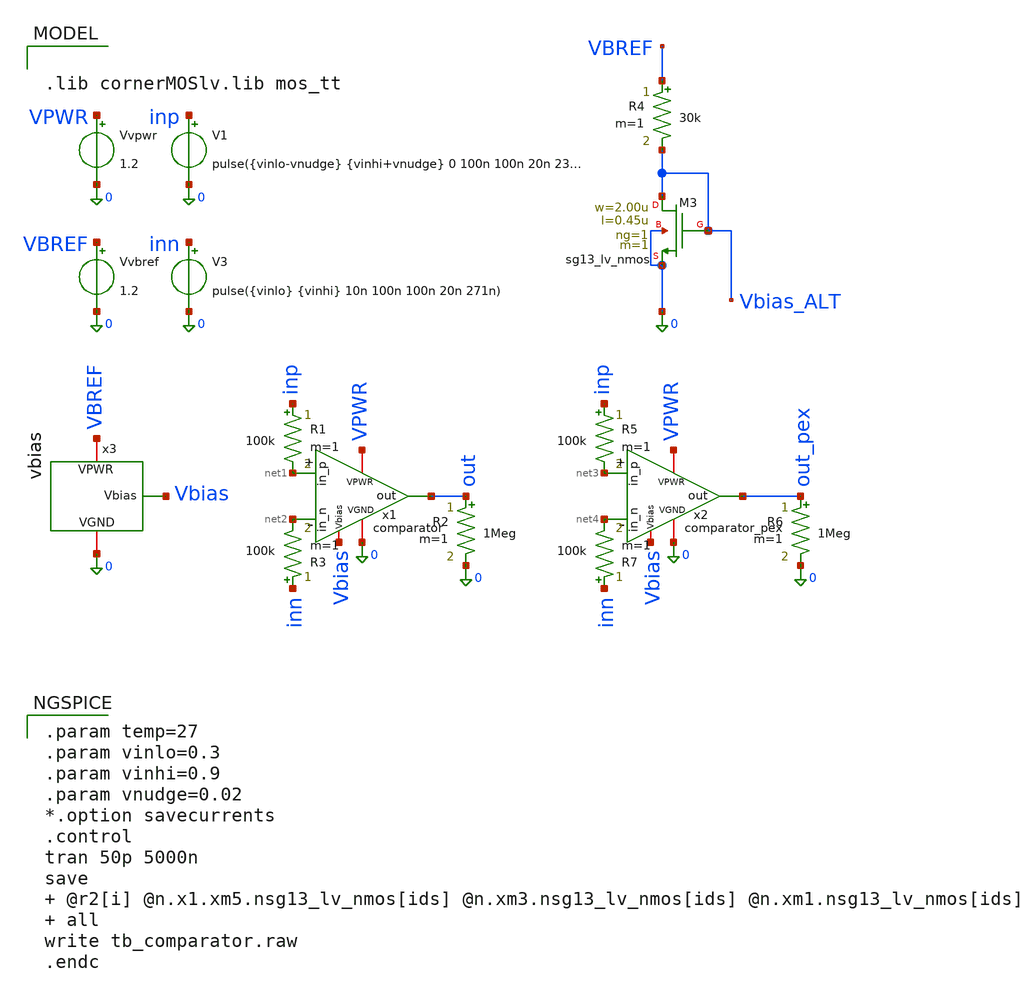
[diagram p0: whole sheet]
** sch_path: xschem/tb_comparator.sch
**.subckt tb_comparator
V1 inp 0 pulse({vinlo-vnudge} {vinhi+vnudge} 0 100n 100n 20n 239n)
R1 inp net1 100k m=1
R2 out 0 1Meg m=1
Vvpwr VPWR 0 1.2
x1 VPWR 0 out net2 net1 Vbias comparator
R3 inn net2 100k m=1
V3 inn 0 pulse({vinlo} {vinhi} 10n 100n 100n 20n 271n)
XM3 Vbias_ALT Vbias_ALT 0 0 sg13_lv_nmos w=2.00u l=0.45u ng=1 m=1 mm_ok=1
Vvbref VBREF 0 1.2
R4 VBREF Vbias_ALT 30k m=1
R5 inp net3 100k m=1
R6 out_pex 0 1Meg m=1
x2 VPWR 0 out_pex net4 net3 Vbias comparator_pex
R7 inn net4 100k m=1
x3 VBREF 0 Vbias vbias
**** begin user architecture code

.lib cornerMOSlv.lib mos_tt


.param temp=27
.param vinlo=0.3
.param vinhi=0.9
.param vnudge=0.02
*.option savecurrents
.control
tran 50p 5000n
save  @r2[i] @n.x1.xm5.nsg13_lv_nmos[ids] @n.xm3.nsg13_lv_nmos[ids] @n.xm1.nsg13_lv_nmos[ids]  all
write tb_comparator.raw
.endc


**** end user architecture code
**.ends

* expanding   symbol:  comparator.sym # of pins=6
** sym_path: xschem/comparator.sym
** sch_path: xschem/comparator.sch
.subckt comparator VPWR VGND out in_n in_p Vbias
*.iopin VPWR
*.ipin in_p
*.ipin in_n
*.opin out
*.iopin VGND
*.ipin Vbias
XM1 net2 in_p net1 VGND sg13_lv_nmos w=4.00u l=0.26u ng=1 m=1 mm_ok=1
XM4 diff net2 VPWR VPWR sg13_lv_pmos w=8.00u l=0.26u ng=1 m=1 mm_ok=1
XM5 net1 Vbias VGND VGND sg13_lv_nmos w=2.00u l=0.39u ng=1 m=1 mm_ok=1
XM2 diff in_n net1 VGND sg13_lv_nmos w=4.00u l=0.26u ng=1 m=1 mm_ok=1
XM3 net2 net2 VPWR VPWR sg13_lv_pmos w=8.00u l=0.26u ng=1 m=1 mm_ok=1
XM6 diff_amp diff VPWR VPWR sg13_lv_pmos w=8.00u l=0.26u ng=1 m=1 mm_ok=1
XM7 diff_amp Vbias VGND VGND sg13_lv_nmos w=2.00u l=0.39u ng=1 m=1 mm_ok=1
XM8 out diff_amp VPWR VPWR sg13_lv_pmos w=1.20u l=0.13u ng=1 m=1 mm_ok=1
XM9 out diff_amp VGND VGND sg13_lv_nmos w=0.50u l=0.13u ng=1 m=1 mm_ok=1
.ends


* expanding   symbol:  comparator_pex.sym # of pins=6
** sym_path: xschem/comparator.sym
.include [file normalize ../magic/comparator.sim.spice]

* expanding   symbol:  vbias.sym # of pins=3
** sym_path: xschem/vbias.sym
** sch_path: xschem/vbias.sch
.subckt vbias VPWR VGND Vbias
*.iopin VPWR
*.opin Vbias
*.iopin VGND
XM1 Vbias Vbias VGND VGND sg13_lv_nmos w=2.00u l=0.45u ng=1 m=1 mm_ok=1
XM2 Vbias Vbias VPWR VPWR sg13_lv_pmos w=1.00u l=0.30u ng=1 m=1 mm_ok=1
.ends

.end
